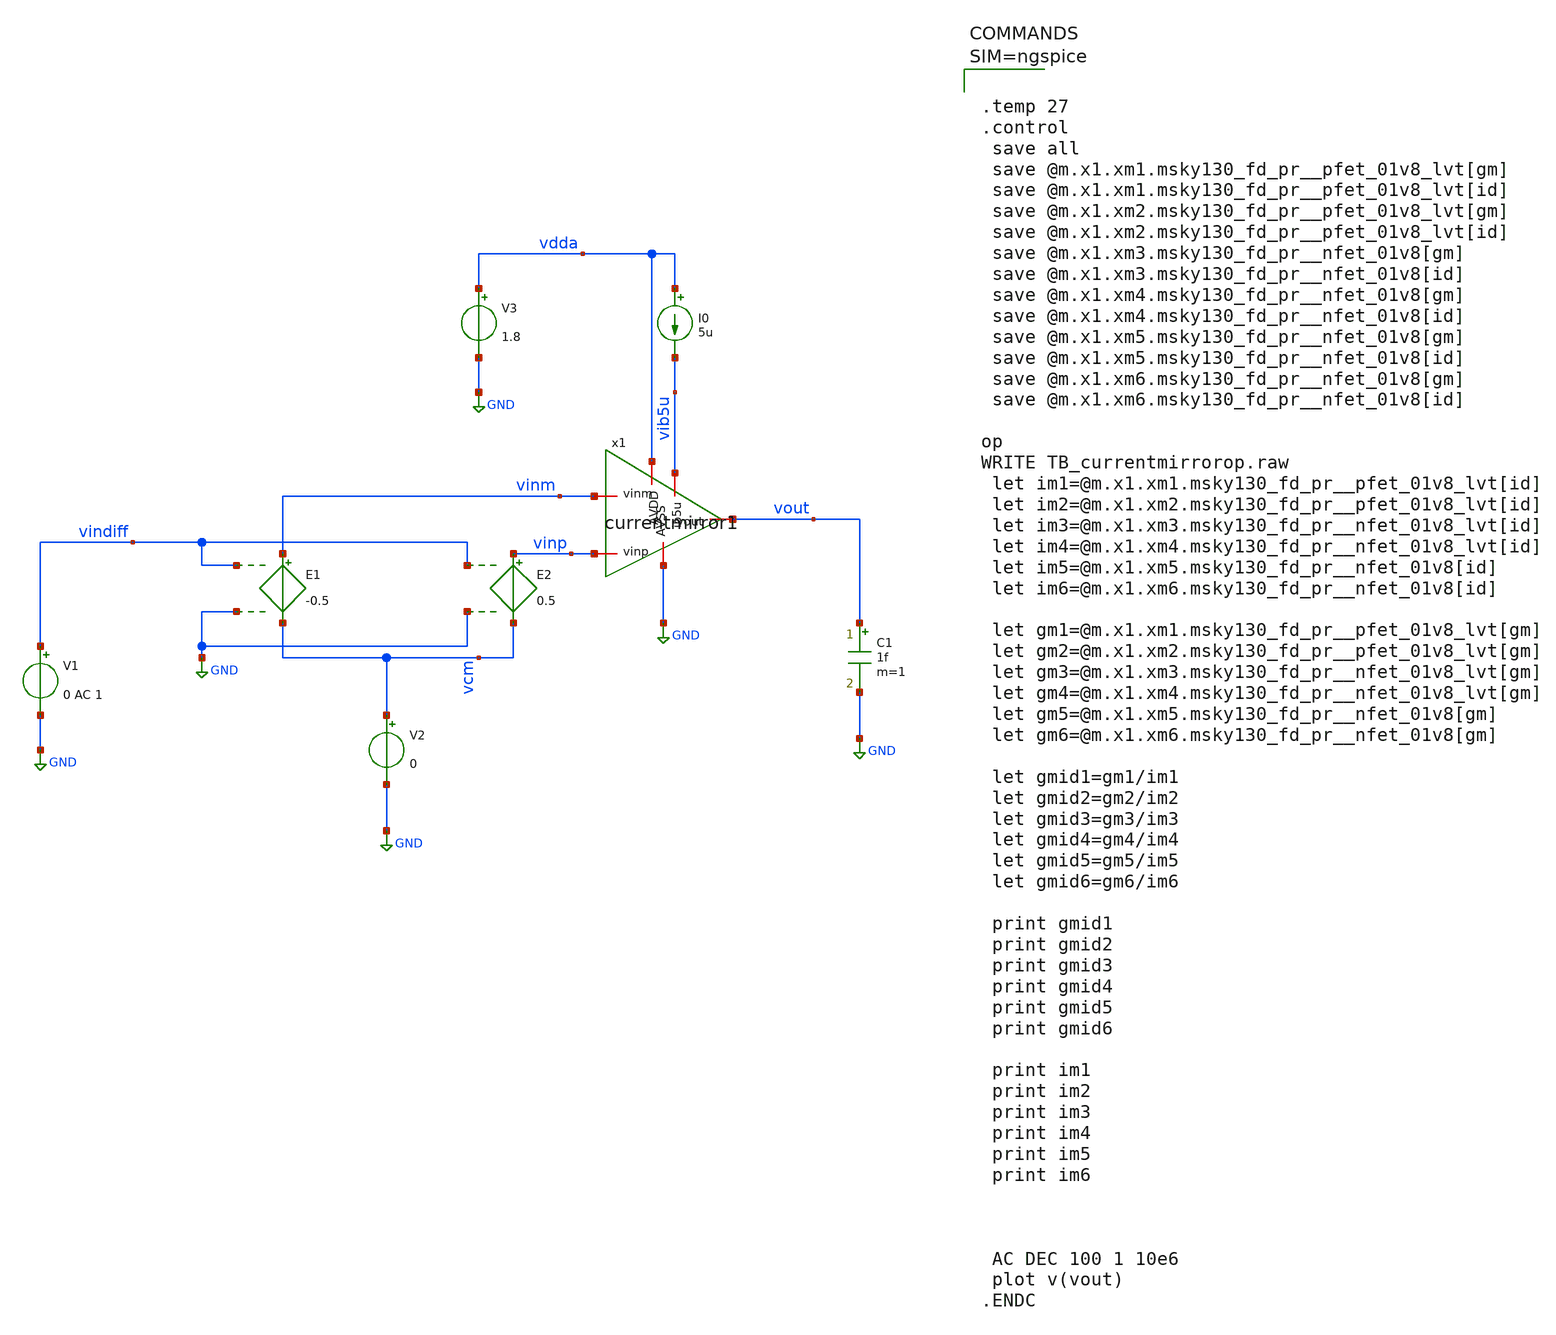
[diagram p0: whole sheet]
** sch_path: xschem/TB_currentmirrorop.sch
**.subckt TB_currentmirrorop
E1 vinm vcm vindiff GND -0.5
E2 vinp vcm vindiff GND 0.5
V1 vindiff GND 0 AC 1
V2 vcm GND 0
V3 vdda GND 1.8
I0 vdda vib5u 5u
C1 vout GND 1f m=1
x1 vdda vout vinm vinp vib5u GND currentmirror1
**** begin user architecture code

** opencircuitdesign pdks install
.lib $::SKYWATER_MODELS/sky130.lib.spice tt




.temp 27
.control
 save all
 save @m.x1.xm1.msky130_fd_pr__pfet_01v8_lvt[gm]
 save @m.x1.xm1.msky130_fd_pr__pfet_01v8_lvt[id]
 save @m.x1.xm2.msky130_fd_pr__pfet_01v8_lvt[gm]
 save @m.x1.xm2.msky130_fd_pr__pfet_01v8_lvt[id]
 save @m.x1.xm3.msky130_fd_pr__nfet_01v8[gm]
 save @m.x1.xm3.msky130_fd_pr__nfet_01v8[id]
 save @m.x1.xm4.msky130_fd_pr__nfet_01v8[gm]
 save @m.x1.xm4.msky130_fd_pr__nfet_01v8[id]
 save @m.x1.xm5.msky130_fd_pr__nfet_01v8[gm]
 save @m.x1.xm5.msky130_fd_pr__nfet_01v8[id]
 save @m.x1.xm6.msky130_fd_pr__nfet_01v8[gm]
 save @m.x1.xm6.msky130_fd_pr__nfet_01v8[id]

op
WRITE TB_currentmirrorop.raw
 let im1=@m.x1.xm1.msky130_fd_pr__pfet_01v8_lvt[id]
 let im2=@m.x1.xm2.msky130_fd_pr__pfet_01v8_lvt[id]
 let im3=@m.x1.xm3.msky130_fd_pr__nfet_01v8_lvt[id]
 let im4=@m.x1.xm4.msky130_fd_pr__nfet_01v8_lvt[id]
 let im5=@m.x1.xm5.msky130_fd_pr__nfet_01v8[id]
 let im6=@m.x1.xm6.msky130_fd_pr__nfet_01v8[id]

 let gm1=@m.x1.xm1.msky130_fd_pr__pfet_01v8_lvt[gm]
 let gm2=@m.x1.xm2.msky130_fd_pr__pfet_01v8_lvt[gm]
 let gm3=@m.x1.xm3.msky130_fd_pr__nfet_01v8_lvt[gm]
 let gm4=@m.x1.xm4.msky130_fd_pr__nfet_01v8_lvt[gm]
 let gm5=@m.x1.xm5.msky130_fd_pr__nfet_01v8[gm]
 let gm6=@m.x1.xm6.msky130_fd_pr__nfet_01v8[gm]

 let gmid1=gm1/im1
 let gmid2=gm2/im2
 let gmid3=gm3/im3
 let gmid4=gm4/im4
 let gmid5=gm5/im5
 let gmid6=gm6/im6

 print gmid1
 print gmid2
 print gmid3
 print gmid4
 print gmid5
 print gmid6

 print im1
 print im2
 print im3
 print im4
 print im5
 print im6



 AC DEC 100 1 10e6
 plot v(vout)
.ENDC



**** end user architecture code
**.ends

* expanding   symbol:  currentmirror1.sym # of pins=6
** sym_path: xschem/currentmirror1.sym
** sch_path: xschem/currentmirror1.sch
.subckt currentmirror1 AVDD vout vinm vinp ib5u AVSS
*.iopin vinp
*.iopin vinm
*.iopin AVDD
*.iopin AVSS
*.iopin ib5u
*.iopin vout
XM5 ib5u ib5u AVSS AVSS sky130_fd_pr__nfet_01v8 L=1 W=5 nf=1 ad='int((1 + 1)/2) * 5 / 1 * 0.29' as='int((1 + 2)/2) * 5 / 1 * 0.29'
+ pd='2*int((1 + 1)/2) * (5 / 1 + 0.29)' ps='2*int((1 + 2)/2) * (5 / 1 + 0.29)' nrd='0.29 / 5 ' nrs='0.29 / 5 '
+ sa=0 sb=0 sd=0 mult=1 m=1
XM6 net1 ib5u AVSS AVSS sky130_fd_pr__nfet_01v8 L=1 W=5 nf=1 ad='int((1 + 1)/2) * 5 / 1 * 0.29' as='int((1 + 2)/2) * 5 / 1 * 0.29'
+ pd='2*int((1 + 1)/2) * (5 / 1 + 0.29)' ps='2*int((1 + 2)/2) * (5 / 1 + 0.29)' nrd='0.29 / 5 ' nrs='0.29 / 5 '
+ sa=0 sb=0 sd=0 mult=2 m=2
XM3 net2 vinp net1 net1 sky130_fd_pr__nfet_01v8 L=2 W=5 nf=1 ad='int((1 + 1)/2) * 5 / 1 * 0.29' as='int((1 + 2)/2) * 5 / 1 * 0.29'
+ pd='2*int((1 + 1)/2) * (5 / 1 + 0.29)' ps='2*int((1 + 2)/2) * (5 / 1 + 0.29)' nrd='0.29 / 5 ' nrs='0.29 / 5 '
+ sa=0 sb=0 sd=0 mult=4 m=4
XM4 vout vinm net1 net1 sky130_fd_pr__nfet_01v8 L=2 W=5 nf=1 ad='int((1 + 1)/2) * 5 / 1 * 0.29' as='int((1 + 2)/2) * 5 / 1 * 0.29'
+ pd='2*int((1 + 1)/2) * (5 / 1 + 0.29)' ps='2*int((1 + 2)/2) * (5 / 1 + 0.29)' nrd='0.29 / 5 ' nrs='0.29 / 5 '
+ sa=0 sb=0 sd=0 mult=4 m=4
XM1 net2 net2 AVDD AVDD sky130_fd_pr__pfet_01v8_lvt L=2 W=5 nf=1 ad='int((1 + 1)/2) * 5 / 1 * 0.29' as='int((1 + 2)/2) * 5 / 1 * 0.29'
+ pd='2*int((1 + 1)/2) * (5 / 1 + 0.29)' ps='2*int((1 + 2)/2) * (5 / 1 + 0.29)' nrd='0.29 / 5 ' nrs='0.29 / 5 '
+ sa=0 sb=0 sd=0 mult=2 m=2
XM2 vout net2 AVDD AVDD sky130_fd_pr__pfet_01v8_lvt L=2 W=5 nf=1 ad='int((1 + 1)/2) * 5 / 1 * 0.29' as='int((1 + 2)/2) * 5 / 1 * 0.29'
+ pd='2*int((1 + 1)/2) * (5 / 1 + 0.29)' ps='2*int((1 + 2)/2) * (5 / 1 + 0.29)' nrd='0.29 / 5 ' nrs='0.29 / 5 '
+ sa=0 sb=0 sd=0 mult=2 m=2
.ends

.GLOBAL GND
.end
